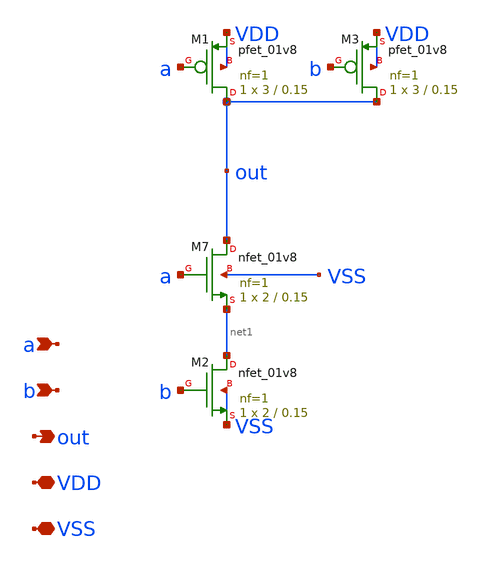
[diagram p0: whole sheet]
** sch_path: xschem/nand_gate.sch
**.subckt nand_gate VDD a out VSS b
*.iopin VDD
*.ipin a
*.opin out
*.iopin VSS
*.ipin b
XM7 out a net1 VSS sky130_fd_pr__nfet_01v8 L=0.15 W=2 nf=1 ad='int((nf+1)/2) * W/nf * 0.29' as='int((nf+2)/2) * W/nf * 0.29'
+ pd='2*int((nf+1)/2) * (W/nf + 0.29)' ps='2*int((nf+2)/2) * (W/nf + 0.29)' nrd='0.29 / W' nrs='0.29 / W'
+ sa=0 sb=0 sd=0 mult=1 m=1
XM1 out a VDD VDD sky130_fd_pr__pfet_01v8 L=0.15 W=3 nf=1 ad='int((nf+1)/2) * W/nf * 0.29' as='int((nf+2)/2) * W/nf * 0.29'
+ pd='2*int((nf+1)/2) * (W/nf + 0.29)' ps='2*int((nf+2)/2) * (W/nf + 0.29)' nrd='0.29 / W' nrs='0.29 / W'
+ sa=0 sb=0 sd=0 mult=1 m=1
XM2 net1 b VSS VSS sky130_fd_pr__nfet_01v8 L=0.15 W=2 nf=1 ad='int((nf+1)/2) * W/nf * 0.29' as='int((nf+2)/2) * W/nf * 0.29'
+ pd='2*int((nf+1)/2) * (W/nf + 0.29)' ps='2*int((nf+2)/2) * (W/nf + 0.29)' nrd='0.29 / W' nrs='0.29 / W'
+ sa=0 sb=0 sd=0 mult=1 m=1
XM3 out b VDD VDD sky130_fd_pr__pfet_01v8 L=0.15 W=3 nf=1 ad='int((nf+1)/2) * W/nf * 0.29' as='int((nf+2)/2) * W/nf * 0.29'
+ pd='2*int((nf+1)/2) * (W/nf + 0.29)' ps='2*int((nf+2)/2) * (W/nf + 0.29)' nrd='0.29 / W' nrs='0.29 / W'
+ sa=0 sb=0 sd=0 mult=1 m=1
**.ends
.end
